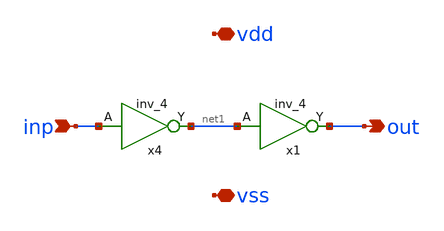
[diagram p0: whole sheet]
** sch_path: xschem/dual_inverter.sch
**.subckt dual_inverter vdd vss inp out
*.iopin vdd
*.iopin vss
*.ipin inp
*.opin out
x4 inp VSS VSS VDD VDD net1 sky130_fd_sc_hd__inv_4
x1 net1 VSS VSS VDD VDD out sky130_fd_sc_hd__inv_4
**.ends
.end
